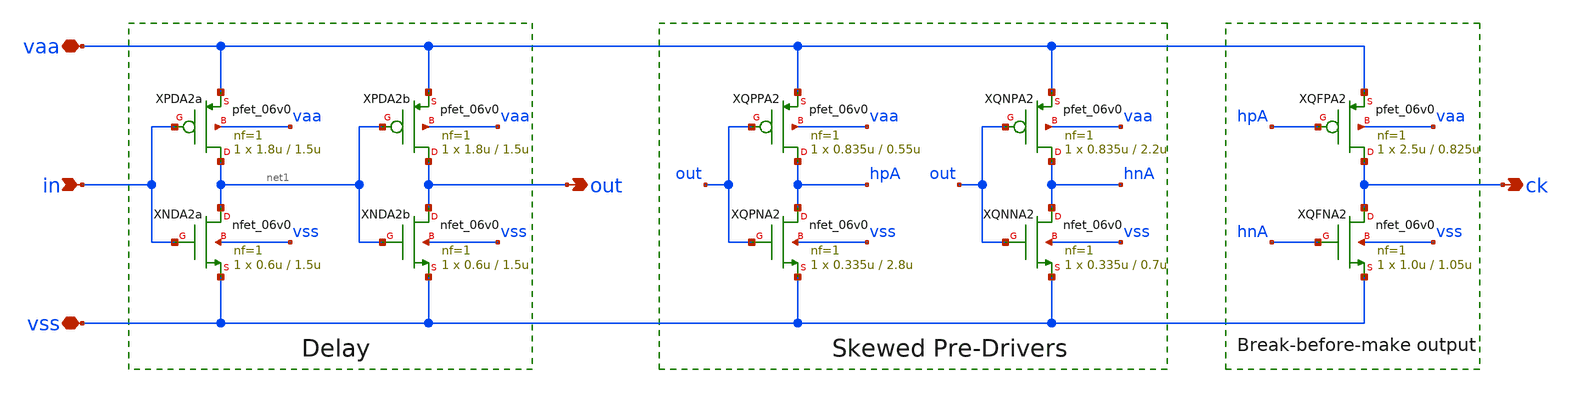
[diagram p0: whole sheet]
** sch_path: xschem/drv_ph.sch
**.subckt drv_ph vaa vss in out ck
*.iopin vaa
*.iopin vss
*.ipin in
*.opin out
*.opin ck
XPDA2a net1 in vaa vaa pfet_06v0 L=1.5u W=1.8u nf=1 ad='int((nf+1)/2) * W/nf * 0.18u' as='int((nf+2)/2) * W/nf * 0.18u'
+ pd='2*int((nf+1)/2) * (W/nf + 0.18u)' ps='2*int((nf+2)/2) * (W/nf + 0.18u)' nrd='0.18u / W' nrs='0.18u / W'
+ sa=0 sb=0 sd=0 m=1
XNDA2a net1 in vss vss nfet_06v0 L=1.5u W=0.6u nf=1 ad='int((nf+1)/2) * W/nf * 0.18u' as='int((nf+2)/2) * W/nf * 0.18u'
+ pd='2*int((nf+1)/2) * (W/nf + 0.18u)' ps='2*int((nf+2)/2) * (W/nf + 0.18u)' nrd='0.18u / W' nrs='0.18u / W'
+ sa=0 sb=0 sd=0 m=1 par=1
XPDA2b out net1 vaa vaa pfet_06v0 L=1.5u W=1.8u nf=1 ad='int((nf+1)/2) * W/nf * 0.18u' as='int((nf+2)/2) * W/nf * 0.18u'
+ pd='2*int((nf+1)/2) * (W/nf + 0.18u)' ps='2*int((nf+2)/2) * (W/nf + 0.18u)' nrd='0.18u / W' nrs='0.18u / W'
+ sa=0 sb=0 sd=0 m=1
XNDA2b out net1 vss vss nfet_06v0 L=1.5u W=0.6u nf=1 ad='int((nf+1)/2) * W/nf * 0.18u' as='int((nf+2)/2) * W/nf * 0.18u'
+ pd='2*int((nf+1)/2) * (W/nf + 0.18u)' ps='2*int((nf+2)/2) * (W/nf + 0.18u)' nrd='0.18u / W' nrs='0.18u / W'
+ sa=0 sb=0 sd=0 m=1 par=1
XQPPA2 hpA out vaa vaa pfet_06v0 L=0.55u W=0.835u nf=1 ad='int((nf+1)/2) * W/nf * 0.18u' as='int((nf+2)/2) * W/nf * 0.18u'
+ pd='2*int((nf+1)/2) * (W/nf + 0.18u)' ps='2*int((nf+2)/2) * (W/nf + 0.18u)' nrd='0.18u / W' nrs='0.18u / W'
+ sa=0 sb=0 sd=0 m=1
XQPNA2 hpA out vss vss nfet_06v0 L=2.8u W=0.335u nf=1 ad='int((nf+1)/2) * W/nf * 0.18u' as='int((nf+2)/2) * W/nf * 0.18u'
+ pd='2*int((nf+1)/2) * (W/nf + 0.18u)' ps='2*int((nf+2)/2) * (W/nf + 0.18u)' nrd='0.18u / W' nrs='0.18u / W'
+ sa=0 sb=0 sd=0 m=1 par=1
XQNPA2 hnA out vaa vaa pfet_06v0 L=2.2u W=0.835u nf=1 ad='int((nf+1)/2) * W/nf * 0.18u' as='int((nf+2)/2) * W/nf * 0.18u'
+ pd='2*int((nf+1)/2) * (W/nf + 0.18u)' ps='2*int((nf+2)/2) * (W/nf + 0.18u)' nrd='0.18u / W' nrs='0.18u / W'
+ sa=0 sb=0 sd=0 m=1
XQNNA2 hnA out vss vss nfet_06v0 L=0.7u W=0.335u nf=1 ad='int((nf+1)/2) * W/nf * 0.18u' as='int((nf+2)/2) * W/nf * 0.18u'
+ pd='2*int((nf+1)/2) * (W/nf + 0.18u)' ps='2*int((nf+2)/2) * (W/nf + 0.18u)' nrd='0.18u / W' nrs='0.18u / W'
+ sa=0 sb=0 sd=0 m=1 par=1
XQFPA2 ck hpA vaa vaa pfet_06v0 L=0.825u W=2.5u nf=1 ad='int((nf+1)/2) * W/nf * 0.18u' as='int((nf+2)/2) * W/nf * 0.18u'
+ pd='2*int((nf+1)/2) * (W/nf + 0.18u)' ps='2*int((nf+2)/2) * (W/nf + 0.18u)' nrd='0.18u / W' nrs='0.18u / W'
+ sa=0 sb=0 sd=0 m=1
XQFNA2 ck hnA vss vss nfet_06v0 L=1.05u W=1.0u nf=1 ad='int((nf+1)/2) * W/nf * 0.18u' as='int((nf+2)/2) * W/nf * 0.18u'
+ pd='2*int((nf+1)/2) * (W/nf + 0.18u)' ps='2*int((nf+2)/2) * (W/nf + 0.18u)' nrd='0.18u / W' nrs='0.18u / W'
+ sa=0 sb=0 sd=0 m=1 par=1
**.ends
.end
